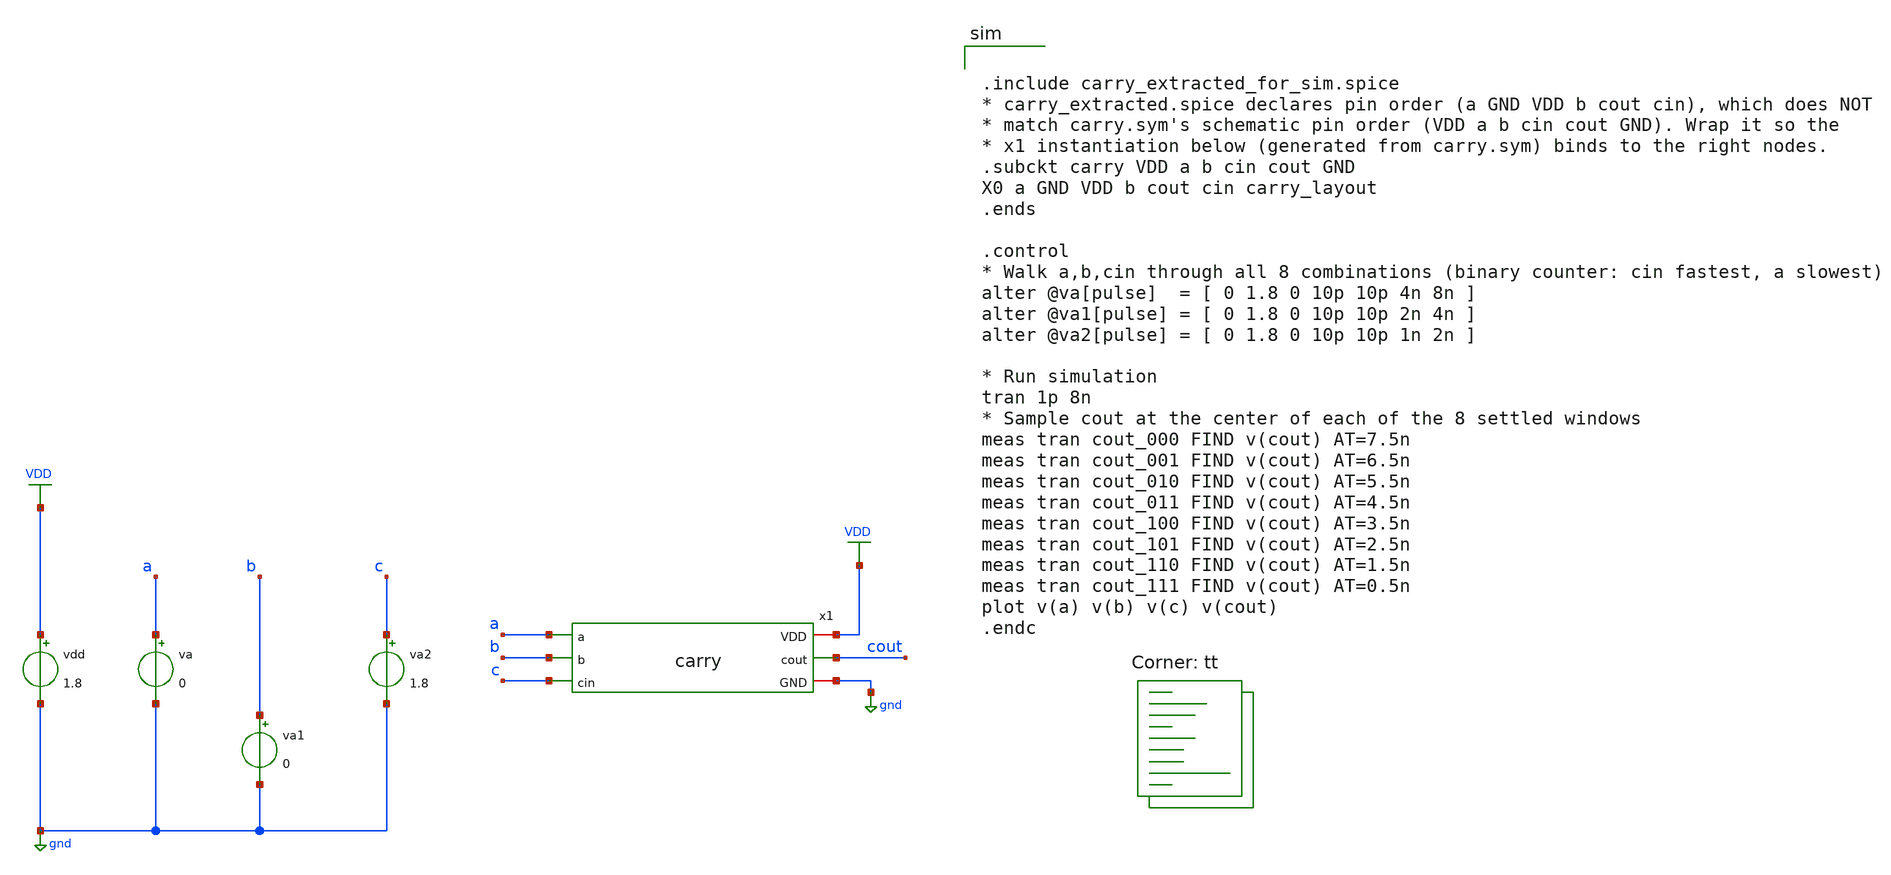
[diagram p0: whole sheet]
** sch_path: assignments/assignment7/carry_tb.sch
**.subckt carry_tb
x1 VDD a b c cout gnd carry
vdd VDD gnd 1.8
va a gnd 0
va1 b gnd 0
va2 c gnd 1.8
**** begin user architecture code


.include carry_extracted_for_sim.spice
* carry_extracted.spice declares pin order (a GND VDD b cout cin), which does NOT
* match carry.sym's schematic pin order (VDD a b cin cout GND). Wrap it so the
* x1 instantiation below (generated from carry.sym) binds to the right nodes.
.subckt carry VDD a b cin cout GND
X0 a GND VDD b cout cin carry_layout
.ends

.control
* Walk a,b,cin through all 8 combinations (binary counter: cin fastest, a slowest)
alter @va[pulse]  = [ 0 1.8 0 10p 10p 4n 8n ]
alter @va1[pulse] = [ 0 1.8 0 10p 10p 2n 4n ]
alter @va2[pulse] = [ 0 1.8 0 10p 10p 1n 2n ]

* Run simulation
tran 1p 8n
* Sample cout at the center of each of the 8 settled windows
meas tran cout_000 FIND v(cout) AT=7.5n
meas tran cout_001 FIND v(cout) AT=6.5n
meas tran cout_010 FIND v(cout) AT=5.5n
meas tran cout_011 FIND v(cout) AT=4.5n
meas tran cout_100 FIND v(cout) AT=3.5n
meas tran cout_101 FIND v(cout) AT=2.5n
meas tran cout_110 FIND v(cout) AT=1.5n
meas tran cout_111 FIND v(cout) AT=0.5n
plot v(a) v(b) v(c) v(cout)
.endc


.lib $::SKYWATER_MODELS/sky130.lib.spice tt
**** end user architecture code
**.ends

* expanding   symbol:  carry.sym # of pins=6
** sym_path: assignments/assignment7/carry.sym
** sch_path: assignments/assignment7/carry.sch
.subckt carry VDD a b cin cout GND
*.opin cout
*.ipin a
*.iopin VDD
*.iopin GND
*.ipin b
*.ipin cin
XM1 cout cin net3 GND sky130_fd_pr__nfet_01v8 L=0.15 W=0.84 nf=2 ad='int((nf+1)/2) * W/nf * 0.29' as='int((nf+2)/2)
+ * W/nf * 0.29' pd='2*int((nf+1)/2) * (W/nf + 0.29)' ps='2*int((nf+2)/2) * (W/nf + 0.29)' nrd='0.29 /
+ W' nrs='0.29 / W' sa=0 sb=0 sd=0 mult=1 m=1
XM2 net1 b VDD VDD sky130_fd_pr__pfet_01v8 L=0.15 W=1.68 nf=4 ad='int((nf+1)/2) * W/nf * 0.29' as='int((nf+2)/2)
+ * W/nf * 0.29' pd='2*int((nf+1)/2) * (W/nf + 0.29)' ps='2*int((nf+2)/2) * (W/nf + 0.29)' nrd='0.29 /
+ W' nrs='0.29 / W' sa=0 sb=0 sd=0 mult=1 m=1
XM3 net3 a GND GND sky130_fd_pr__nfet_01v8 L=0.15 W=0.84 nf=2 ad='int((nf+1)/2) * W/nf * 0.29' as='int((nf+2)/2)
+ * W/nf * 0.29' pd='2*int((nf+1)/2) * (W/nf + 0.29)' ps='2*int((nf+2)/2) * (W/nf + 0.29)' nrd='0.29 /
+ W' nrs='0.29 / W' sa=0 sb=0 sd=0 mult=1 m=1
XM4 cout cin net1 VDD sky130_fd_pr__pfet_01v8 L=0.15 W=1.68 nf=4 ad='int((nf+1)/2) * W/nf * 0.29' as='int((nf+2)/2)
+ * W/nf * 0.29' pd='2*int((nf+1)/2) * (W/nf + 0.29)' ps='2*int((nf+2)/2) * (W/nf + 0.29)' nrd='0.29 /
+ W' nrs='0.29 / W' sa=0 sb=0 sd=0 mult=1 m=1
XM5 net1 a VDD VDD sky130_fd_pr__pfet_01v8 L=0.15 W=1.68 nf=4 ad='int((nf+1)/2) * W/nf * 0.29' as='int((nf+2)/2)
+ * W/nf * 0.29' pd='2*int((nf+1)/2) * (W/nf + 0.29)' ps='2*int((nf+2)/2) * (W/nf + 0.29)' nrd='0.29 /
+ W' nrs='0.29 / W' sa=0 sb=0 sd=0 mult=1 m=1
XM6 net2 a VDD VDD sky130_fd_pr__pfet_01v8 L=0.15 W=1.68 nf=4 ad='int((nf+1)/2) * W/nf * 0.29' as='int((nf+2)/2)
+ * W/nf * 0.29' pd='2*int((nf+1)/2) * (W/nf + 0.29)' ps='2*int((nf+2)/2) * (W/nf + 0.29)' nrd='0.29 /
+ W' nrs='0.29 / W' sa=0 sb=0 sd=0 mult=1 m=1
XM7 cout b net2 VDD sky130_fd_pr__pfet_01v8 L=0.15 W=1.68 nf=4 ad='int((nf+1)/2) * W/nf * 0.29' as='int((nf+2)/2)
+ * W/nf * 0.29' pd='2*int((nf+1)/2) * (W/nf + 0.29)' ps='2*int((nf+2)/2) * (W/nf + 0.29)' nrd='0.29 /
+ W' nrs='0.29 / W' sa=0 sb=0 sd=0 mult=1 m=1
XM8 net3 b GND GND sky130_fd_pr__nfet_01v8 L=0.15 W=0.84 nf=2 ad='int((nf+1)/2) * W/nf * 0.29' as='int((nf+2)/2)
+ * W/nf * 0.29' pd='2*int((nf+1)/2) * (W/nf + 0.29)' ps='2*int((nf+2)/2) * (W/nf + 0.29)' nrd='0.29 /
+ W' nrs='0.29 / W' sa=0 sb=0 sd=0 mult=1 m=1
XM9 cout a net4 GND sky130_fd_pr__nfet_01v8 L=0.15 W=0.84 nf=2 ad='int((nf+1)/2) * W/nf * 0.29' as='int((nf+2)/2)
+ * W/nf * 0.29' pd='2*int((nf+1)/2) * (W/nf + 0.29)' ps='2*int((nf+2)/2) * (W/nf + 0.29)' nrd='0.29 /
+ W' nrs='0.29 / W' sa=0 sb=0 sd=0 mult=1 m=1
XM10 net4 b GND GND sky130_fd_pr__nfet_01v8 L=0.15 W=0.84 nf=2 ad='int((nf+1)/2) * W/nf * 0.29' as='int((nf+2)/2)
+ * W/nf * 0.29' pd='2*int((nf+1)/2) * (W/nf + 0.29)' ps='2*int((nf+2)/2) * (W/nf + 0.29)' nrd='0.29 /
+ W' nrs='0.29 / W' sa=0 sb=0 sd=0 mult=1 m=1
.ends

.GLOBAL gnd
.GLOBAL VDD
.end
